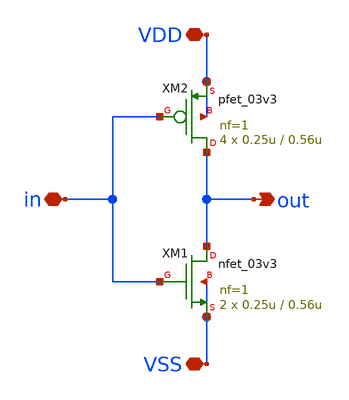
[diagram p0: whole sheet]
** sch_path: designs/sar_adc/digital/buffer_inv_x1/xschem/inverter.sch
**.subckt inverter out in VDD VSS
*.opin out
*.iopin in
*.iopin VDD
*.iopin VSS
XM1 out in VSS VSS nfet_03v3 L=0.56u W=0.25u nf=1 ad='int((nf+1)/2) * W/nf * 0.18u' as='int((nf+2)/2) * W/nf * 0.18u'
+ pd='2*int((nf+1)/2) * (W/nf + 0.18u)' ps='2*int((nf+2)/2) * (W/nf + 0.18u)' nrd='0.18u / W' nrs='0.18u / W'
+ sa=0 sb=0 sd=0 m=2
XM2 out in VDD VDD pfet_03v3 L=0.56u W=0.25u nf=1 ad='int((nf+1)/2) * W/nf * 0.18u' as='int((nf+2)/2) * W/nf * 0.18u'
+ pd='2*int((nf+1)/2) * (W/nf + 0.18u)' ps='2*int((nf+2)/2) * (W/nf + 0.18u)' nrd='0.18u / W' nrs='0.18u / W'
+ sa=0 sb=0 sd=0 m=4
**.ends
.end
